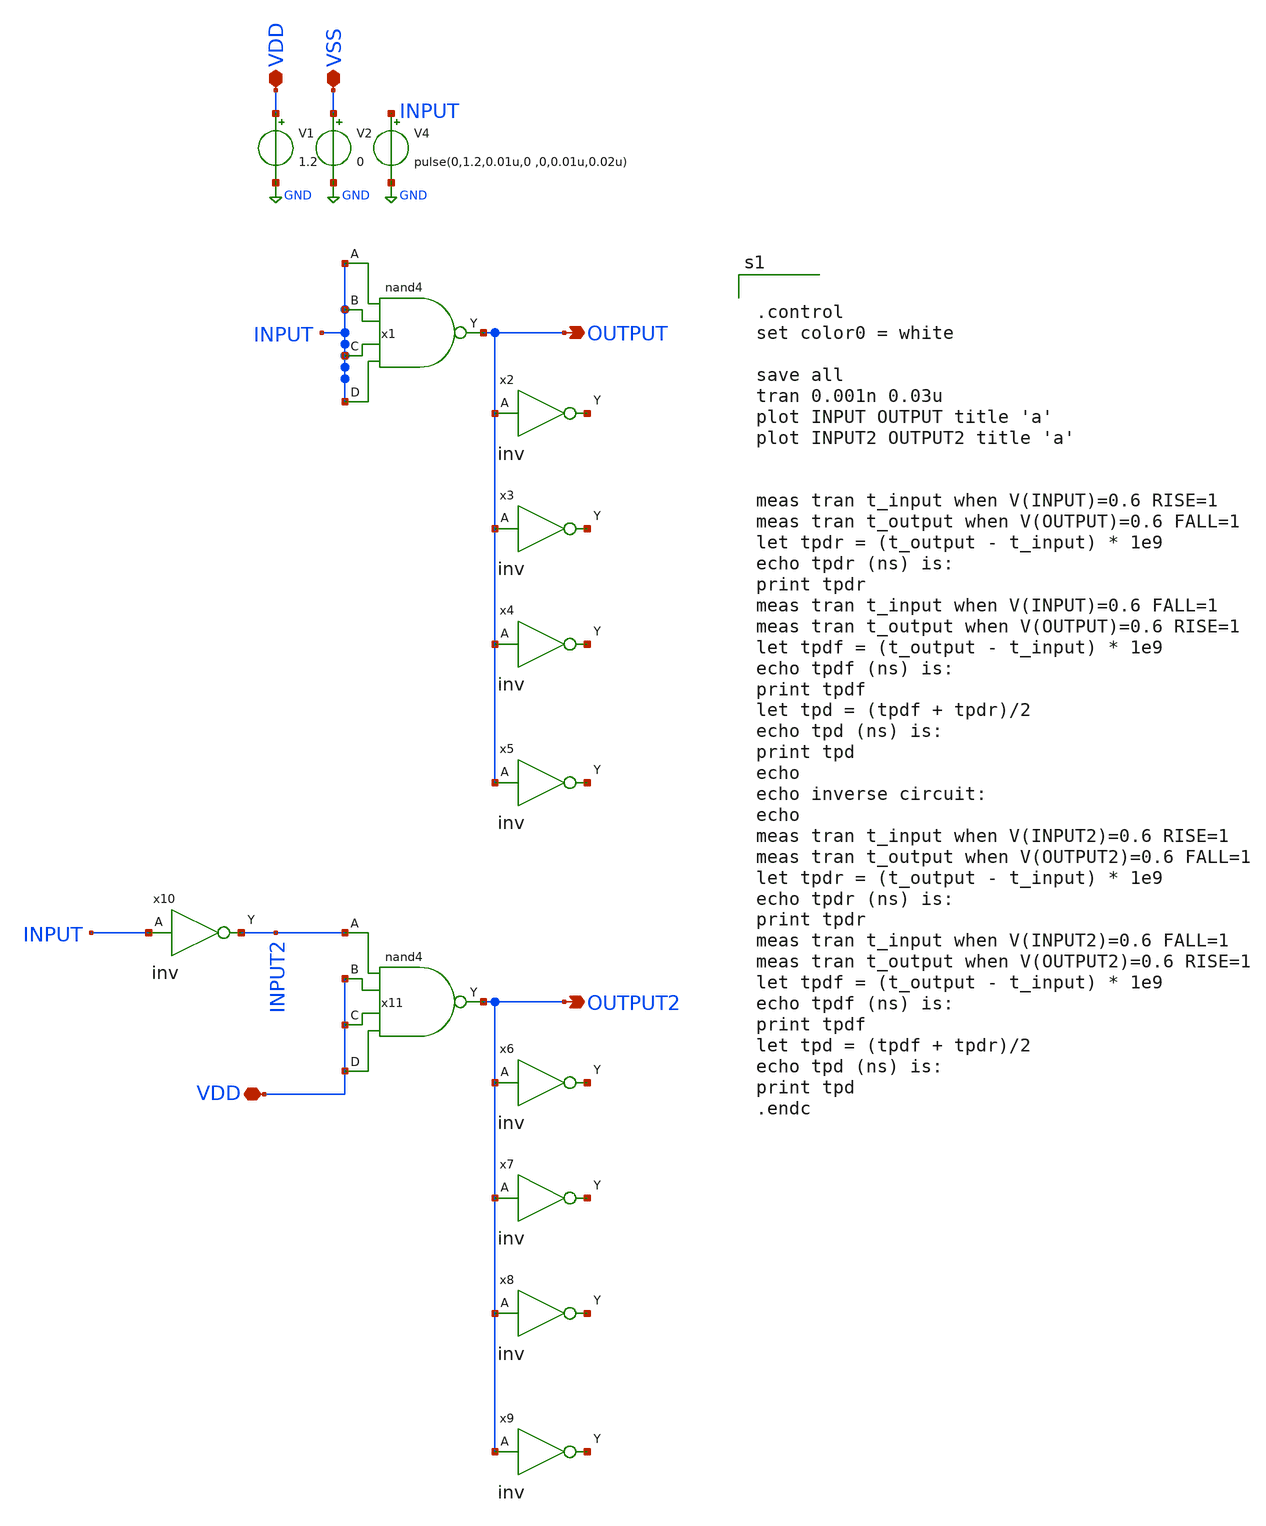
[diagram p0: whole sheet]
** sch_path: design/xschem/NAND/nand4_TB.sch
**.subckt nand4_TB OUTPUT VDD VSS OUTPUT2 VDD
*.opin OUTPUT
*.iopin VDD
*.iopin VSS
*.opin OUTPUT2
*.iopin VDD
V1 VDD GND 1.2
V2 VSS GND 0
V4 INPUT GND pulse(0,1.2,0.01u,0 ,0,0.01u,0.02u)
x2 OUTPUT VSS VDD net1 inv
x3 OUTPUT VSS VDD net2 inv
x4 OUTPUT VSS VDD net3 inv
x5 OUTPUT VSS VDD net4 inv
x6 OUTPUT2 VSS VDD net5 inv
x7 OUTPUT2 VSS VDD net6 inv
x8 OUTPUT2 VSS VDD net7 inv
x9 OUTPUT2 VSS VDD net8 inv
x10 INPUT VSS VDD INPUT2 inv
x1 INPUT INPUT INPUT INPUT VSS VDD OUTPUT nand4
x11 INPUT2 VDD VDD VDD VSS VDD OUTPUT2 nand4
**** begin user architecture code

** opencircuitdesign pdks install
.lib $::SKYWATER_MODELS/sky130.lib.spice tt_mm




.control
set color0 = white

save all
tran 0.001n 0.03u
plot INPUT OUTPUT title 'a'
plot INPUT2 OUTPUT2 title 'a'


meas tran t_input when V(INPUT)=0.6 RISE=1
meas tran t_output when V(OUTPUT)=0.6 FALL=1
let tpdr = (t_output - t_input) * 1e9
echo tpdr (ns) is:
print tpdr
meas tran t_input when V(INPUT)=0.6 FALL=1
meas tran t_output when V(OUTPUT)=0.6 RISE=1
let tpdf = (t_output - t_input) * 1e9
echo tpdf (ns) is:
print tpdf
let tpd = (tpdf + tpdr)/2
echo tpd (ns) is:
print tpd
echo
echo inverse circuit:
echo
meas tran t_input when V(INPUT2)=0.6 RISE=1
meas tran t_output when V(OUTPUT2)=0.6 FALL=1
let tpdr = (t_output - t_input) * 1e9
echo tpdr (ns) is:
print tpdr
meas tran t_input when V(INPUT2)=0.6 FALL=1
meas tran t_output when V(OUTPUT2)=0.6 RISE=1
let tpdf = (t_output - t_input) * 1e9
echo tpdf (ns) is:
print tpdf
let tpd = (tpdf + tpdr)/2
echo tpd (ns) is:
print tpd
.endc


**** end user architecture code
**.ends

* expanding   symbol:  INV/inv.sym # of pins=2
** sym_path: design/xschem/INV/inv.sym
** sch_path: design/xschem/INV/inv.sch
.subckt inv A VSS VDD Y
*.ipin A
*.opin Y
XM2 Y A VSS GND sky130_fd_pr__nfet_01v8 L=0.15 W=1 nf=1 ad='int((nf+1)/2) * W/nf * 0.29' as='int((nf+2)/2) * W/nf * 0.29'
+ pd='2*int((nf+1)/2) * (W/nf + 0.29)' ps='2*int((nf+2)/2) * (W/nf + 0.29)' nrd='0.29 / W' nrs='0.29 / W'
+ sa=0 sb=0 sd=0 mult=1 m=1
XM1 Y A VDD VDD sky130_fd_pr__pfet_01v8 L=0.15 W=3.21 nf=1 ad='int((nf+1)/2) * W/nf * 0.29' as='int((nf+2)/2) * W/nf * 0.29'
+ pd='2*int((nf+1)/2) * (W/nf + 0.29)' ps='2*int((nf+2)/2) * (W/nf + 0.29)' nrd='0.29 / W' nrs='0.29 / W'
+ sa=0 sb=0 sd=0 mult=1 m=1
.ends


* expanding   symbol:  NAND/nand4.sym # of pins=5
** sym_path: design/xschem/NAND/nand4.sym
** sch_path: design/xschem/NAND/nand4.sch
.subckt nand4 A B C D VSS VDD Y
*.ipin A
*.opin Y
*.ipin B
*.ipin C
*.ipin D
XM1 Y A VDD VDD sky130_fd_pr__pfet_01v8 L=0.15 W=3.2 nf=1 ad='int((nf+1)/2) * W/nf * 0.29' as='int((nf+2)/2) * W/nf * 0.29'
+ pd='2*int((nf+1)/2) * (W/nf + 0.29)' ps='2*int((nf+2)/2) * (W/nf + 0.29)' nrd='0.29 / W' nrs='0.29 / W'
+ sa=0 sb=0 sd=0 mult=1 m=1
XM2 Y A net1 net1 sky130_fd_pr__nfet_01v8 L=0.15 W=1 nf=1 ad='int((nf+1)/2) * W/nf * 0.29' as='int((nf+2)/2) * W/nf * 0.29'
+ pd='2*int((nf+1)/2) * (W/nf + 0.29)' ps='2*int((nf+2)/2) * (W/nf + 0.29)' nrd='0.29 / W' nrs='0.29 / W'
+ sa=0 sb=0 sd=0 mult=1 m=1
XM3 net1 B net2 net2 sky130_fd_pr__nfet_01v8 L=0.15 W=1 nf=1 ad='int((nf+1)/2) * W/nf * 0.29' as='int((nf+2)/2) * W/nf * 0.29'
+ pd='2*int((nf+1)/2) * (W/nf + 0.29)' ps='2*int((nf+2)/2) * (W/nf + 0.29)' nrd='0.29 / W' nrs='0.29 / W'
+ sa=0 sb=0 sd=0 mult=1 m=1
XM4 Y B VDD VDD sky130_fd_pr__pfet_01v8 L=0.15 W=3.2 nf=1 ad='int((nf+1)/2) * W/nf * 0.29' as='int((nf+2)/2) * W/nf * 0.29'
+ pd='2*int((nf+1)/2) * (W/nf + 0.29)' ps='2*int((nf+2)/2) * (W/nf + 0.29)' nrd='0.29 / W' nrs='0.29 / W'
+ sa=0 sb=0 sd=0 mult=1 m=1
XM5 Y C VDD VDD sky130_fd_pr__pfet_01v8 L=0.15 W=3.2 nf=1 ad='int((nf+1)/2) * W/nf * 0.29' as='int((nf+2)/2) * W/nf * 0.29'
+ pd='2*int((nf+1)/2) * (W/nf + 0.29)' ps='2*int((nf+2)/2) * (W/nf + 0.29)' nrd='0.29 / W' nrs='0.29 / W'
+ sa=0 sb=0 sd=0 mult=1 m=1
XM6 net2 C net3 net3 sky130_fd_pr__nfet_01v8 L=0.15 W=1 nf=1 ad='int((nf+1)/2) * W/nf * 0.29' as='int((nf+2)/2) * W/nf * 0.29'
+ pd='2*int((nf+1)/2) * (W/nf + 0.29)' ps='2*int((nf+2)/2) * (W/nf + 0.29)' nrd='0.29 / W' nrs='0.29 / W'
+ sa=0 sb=0 sd=0 mult=1 m=1
XM7 net3 D VSS VSS sky130_fd_pr__nfet_01v8 L=0.15 W=1 nf=1 ad='int((nf+1)/2) * W/nf * 0.29' as='int((nf+2)/2) * W/nf * 0.29'
+ pd='2*int((nf+1)/2) * (W/nf + 0.29)' ps='2*int((nf+2)/2) * (W/nf + 0.29)' nrd='0.29 / W' nrs='0.29 / W'
+ sa=0 sb=0 sd=0 mult=1 m=1
XM8 Y D VDD VDD sky130_fd_pr__pfet_01v8 L=0.15 W=3.2 nf=1 ad='int((nf+1)/2) * W/nf * 0.29' as='int((nf+2)/2) * W/nf * 0.29'
+ pd='2*int((nf+1)/2) * (W/nf + 0.29)' ps='2*int((nf+2)/2) * (W/nf + 0.29)' nrd='0.29 / W' nrs='0.29 / W'
+ sa=0 sb=0 sd=0 mult=1 m=1
.ends

.GLOBAL GND
.end
